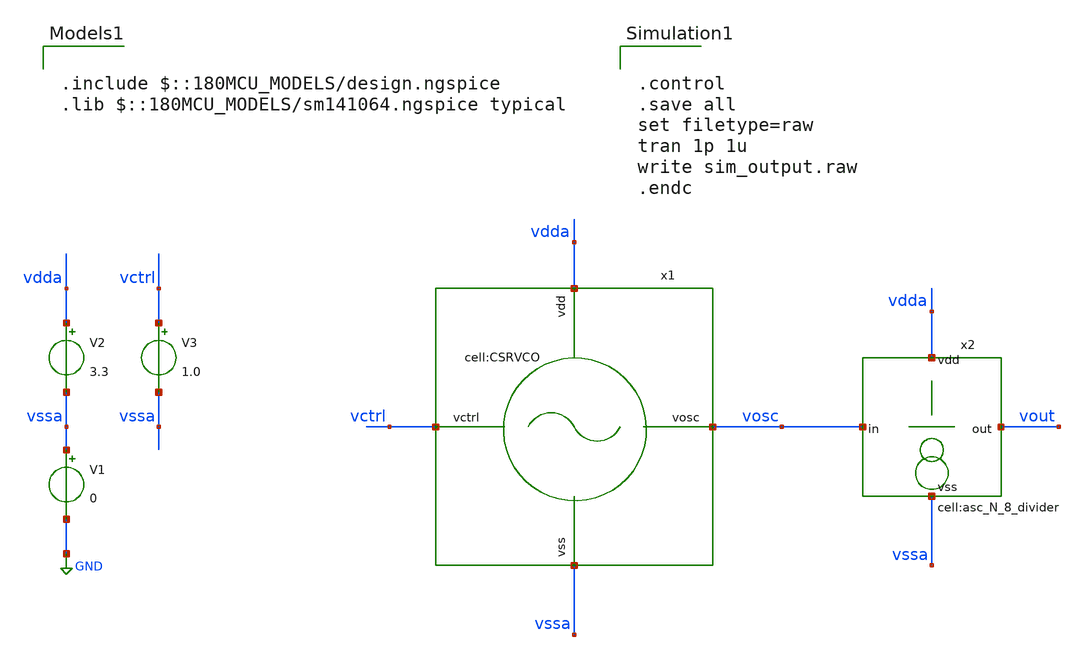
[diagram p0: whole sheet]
** sch_path: designs/libs/xp_tb_analog/tb_vco_plus_divider/tb_vco_plus_divider.sch
**.subckt tb_vco_plus_divider
x1 vctrl vdda vssa vosc CSRVCO
V1 vssa GND 0
V2 vdda vssa 3.3
V3 vctrl vssa 1.0
x2 vosc vout vdda vssa asc_N_8_divider
**** begin user architecture code

.include $::180MCU_MODELS/design.ngspice
.lib $::180MCU_MODELS/sm141064.ngspice typical



.control
.save all
set filetype=raw
tran 1p 1u
write sim_output.raw
.endc


**** end user architecture code
**.ends
.GLOBAL GND
.end
